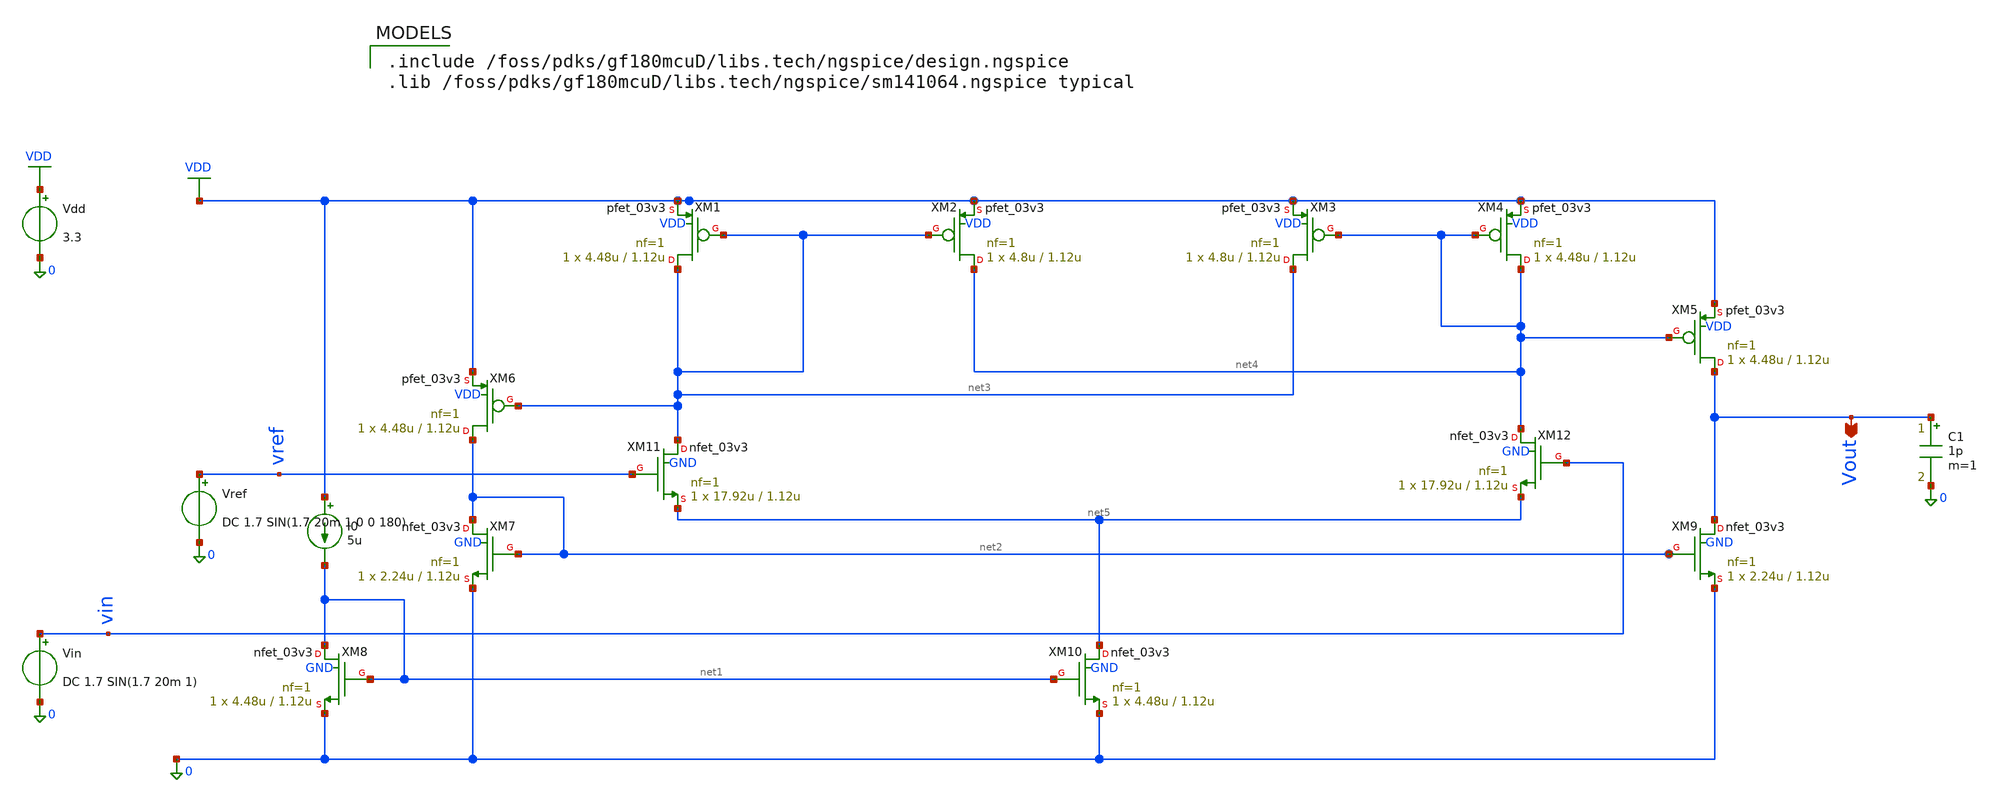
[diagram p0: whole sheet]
** sch_path: comparator/schematic-design/coc_sim2.sch
**.subckt coc_sim2 Vout
*.opin Vout
XM1 net3 net3 VDD VDD pfet_03v3 L=1.12u W=4.48u nf=1 ad='int((nf+1)/2) * W/nf * 0.18u' as='int((nf+2)/2) * W/nf * 0.18u'
+ pd='2*int((nf+1)/2) * (W/nf + 0.18u)' ps='2*int((nf+2)/2) * (W/nf + 0.18u)' nrd='0.18u / W' nrs='0.18u / W'
+ sa=0 sb=0 sd=0 m=1 par=1
XM2 net4 net3 VDD VDD pfet_03v3 L=1.12u W=4.8u nf=1 ad='int((nf+1)/2) * W/nf * 0.18u' as='int((nf+2)/2) * W/nf * 0.18u'
+ pd='2*int((nf+1)/2) * (W/nf + 0.18u)' ps='2*int((nf+2)/2) * (W/nf + 0.18u)' nrd='0.18u / W' nrs='0.18u / W'
+ sa=0 sb=0 sd=0 m=1 par=1
XM3 net3 net4 VDD VDD pfet_03v3 L=1.12u W=4.8u nf=1 ad='int((nf+1)/2) * W/nf * 0.18u' as='int((nf+2)/2) * W/nf * 0.18u'
+ pd='2*int((nf+1)/2) * (W/nf + 0.18u)' ps='2*int((nf+2)/2) * (W/nf + 0.18u)' nrd='0.18u / W' nrs='0.18u / W'
+ sa=0 sb=0 sd=0 m=1 par=1
XM4 net4 net4 VDD VDD pfet_03v3 L=1.12u W=4.48u nf=1 ad='int((nf+1)/2) * W/nf * 0.18u' as='int((nf+2)/2) * W/nf * 0.18u'
+ pd='2*int((nf+1)/2) * (W/nf + 0.18u)' ps='2*int((nf+2)/2) * (W/nf + 0.18u)' nrd='0.18u / W' nrs='0.18u / W'
+ sa=0 sb=0 sd=0 m=1 par=1
XM5 Vout net4 VDD VDD pfet_03v3 L=1.12u W=4.48u nf=1 ad='int((nf+1)/2) * W/nf * 0.18u' as='int((nf+2)/2) * W/nf * 0.18u'
+ pd='2*int((nf+1)/2) * (W/nf + 0.18u)' ps='2*int((nf+2)/2) * (W/nf + 0.18u)' nrd='0.18u / W' nrs='0.18u / W'
+ sa=0 sb=0 sd=0 m=1 par=1
XM6 net2 net3 VDD VDD pfet_03v3 L=1.12u W=4.48u nf=1 ad='int((nf+1)/2) * W/nf * 0.18u' as='int((nf+2)/2) * W/nf * 0.18u'
+ pd='2*int((nf+1)/2) * (W/nf + 0.18u)' ps='2*int((nf+2)/2) * (W/nf + 0.18u)' nrd='0.18u / W' nrs='0.18u / W'
+ sa=0 sb=0 sd=0 m=1 par=1
XM7 net2 net2 0 GND nfet_03v3 L=1.12u W=2.24u nf=1 ad='int((nf+1)/2) * W/nf * 0.18u' as='int((nf+2)/2) * W/nf * 0.18u'
+ pd='2*int((nf+1)/2) * (W/nf + 0.18u)' ps='2*int((nf+2)/2) * (W/nf + 0.18u)' nrd='0.18u / W' nrs='0.18u / W'
+ sa=0 sb=0 sd=0 m=1 par=1
XM8 net1 net1 0 GND nfet_03v3 L=1.12u W=4.48u nf=1 ad='int((nf+1)/2) * W/nf * 0.18u' as='int((nf+2)/2) * W/nf * 0.18u'
+ pd='2*int((nf+1)/2) * (W/nf + 0.18u)' ps='2*int((nf+2)/2) * (W/nf + 0.18u)' nrd='0.18u / W' nrs='0.18u / W'
+ sa=0 sb=0 sd=0 m=1 par=1
XM9 Vout net2 0 GND nfet_03v3 L=1.12u W=2.24u nf=1 ad='int((nf+1)/2) * W/nf * 0.18u' as='int((nf+2)/2) * W/nf * 0.18u'
+ pd='2*int((nf+1)/2) * (W/nf + 0.18u)' ps='2*int((nf+2)/2) * (W/nf + 0.18u)' nrd='0.18u / W' nrs='0.18u / W'
+ sa=0 sb=0 sd=0 m=1 par=1
XM10 net5 net1 0 GND nfet_03v3 L=1.12u W=4.48u nf=1 ad='int((nf+1)/2) * W/nf * 0.18u' as='int((nf+2)/2) * W/nf * 0.18u'
+ pd='2*int((nf+1)/2) * (W/nf + 0.18u)' ps='2*int((nf+2)/2) * (W/nf + 0.18u)' nrd='0.18u / W' nrs='0.18u / W'
+ sa=0 sb=0 sd=0 m=1 par=1
XM11 net3 vref net5 GND nfet_03v3 L=1.12u W=17.92u nf=1 ad='int((nf+1)/2) * W/nf * 0.18u' as='int((nf+2)/2) * W/nf * 0.18u'
+ pd='2*int((nf+1)/2) * (W/nf + 0.18u)' ps='2*int((nf+2)/2) * (W/nf + 0.18u)' nrd='0.18u / W' nrs='0.18u / W'
+ sa=0 sb=0 sd=0 m=1 par=1
XM12 net4 vin net5 GND nfet_03v3 L=1.12u W=17.92u nf=1 ad='int((nf+1)/2) * W/nf * 0.18u' as='int((nf+2)/2) * W/nf * 0.18u'
+ pd='2*int((nf+1)/2) * (W/nf + 0.18u)' ps='2*int((nf+2)/2) * (W/nf + 0.18u)' nrd='0.18u / W' nrs='0.18u / W'
+ sa=0 sb=0 sd=0 m=1 par=1
I0 VDD net1 5u
Vref vref 0 DC 1.7 SIN(1.7 20m 1 0 0 180)
Vin vin 0 DC 1.7 SIN(1.7 20m 1)

Vdd VDD 0 3.3
C1 Vout 0 1p m=1
**** begin user architecture code

.include /foss/pdks/gf180mcuD/libs.tech/ngspice/design.ngspice
.lib /foss/pdks/gf180mcuD/libs.tech/ngspice/sm141064.ngspice typical


.control

set noaskquit
save v(vin) v(vref) v(vout)

* ============================================================
* COMPARATOR TRANSIENT TEST
* Mimics LPF output:
* Vin = 1.7 V +/- 20 mV = 40 mVpp
* Vref = fixed 1.7 V
* Frequency = 1 Hz
* Expected Vout = ~0 V <-> ~3.3 V
* ============================================================

tran 1m 6

write comparator_sine_40mVpp.raw v(vin) v(vref) v(vout)

plot v(vin) v(vref)
plot v(vout)

.endc


**** end user architecture code
**.ends
.GLOBAL VDD
.end
